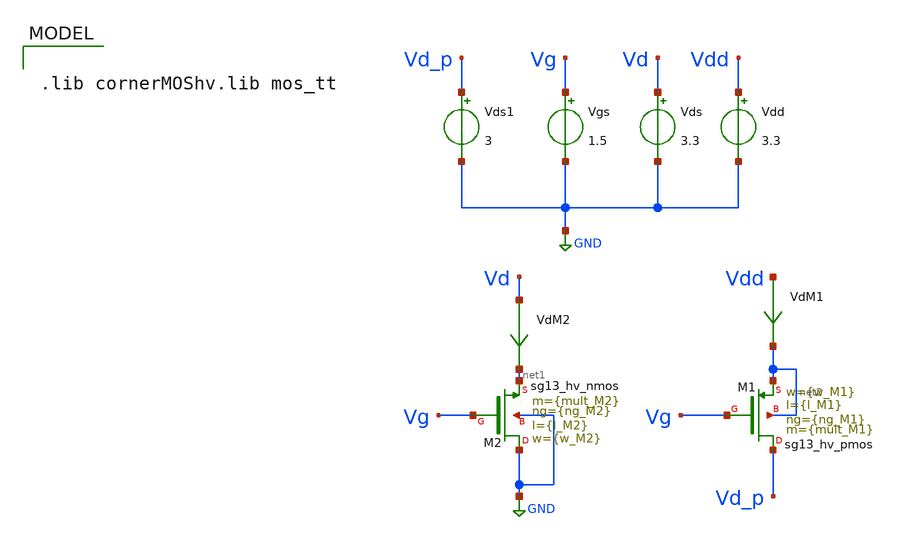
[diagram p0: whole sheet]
** sch_path: xschem/TB_hvMOS_POWER_Sizing.sch
**.subckt TB_hvMOS_POWER_Sizing
Vgs Vg GND 1.5
Vds Vd GND 3.3
Vdd Vdd GND 3.3
XM2 GND Vg net1 GND sg13_hv_nmos w={w_M2} l={l_M2} ng={ng_M2} m={mult_M2} mm_ok=1
VdM1 Vdd net2 0
.save i(vdm1)
XM1 Vd_p Vg net2 net2 sg13_hv_pmos w={w_M1} l={l_M1} ng={ng_M1} m={mult_M1} mm_ok=1
VdM2 Vd net1 0
.save i(vdm2)
Vds1 Vd_p GND 3
**** begin user architecture code

.lib cornerMOShv.lib mos_tt



.save all
* + @M.XM1.m1[id]  @n.xm1.nsg13_hv_pmos[vth]  @n.xm1.nsg13_hv_pmos[ad]  @n.xm2.nsg13_hv_nmos[vth]

.control
reset
alter Vgs 3.3
dc Vds 0 1 0.01
*dc Vds 0 0.5 0.01 temp 0 27 1
let Vds_M2 = v(Vd)
plot i(VdM2) vs Vds_M2

*meas DC Ron_M2 DERIV i(VdM2) AT=0.2
let I_M2 = i(VdM2)
let G_M2 = deriv(I_M2)
let Ron_M2 = 1/G_M2
plot Ron_M2
let VthM1_off =  @n.xm1.nsg13_hv_pmos[vth]
let VthM2 =  @n.xm2.nsg13_hv_nmos[vth]
*plot VthM1_off
*plot VthM2
.endc

.control
reset
alter Vgs 0
dc Vds1 2 3.3 0.01
*dc Vds 2 3.3 0.01 temp 0 27 1

plot i(VdM1)
let I_M1 = i(VdM1)
let G_M1 = deriv(I_M1)
let Ron_M1 = -1/G_M1
let Vsd_M1 = v(Vdd) -v(Vd_p)
plot Ron_M1 vs Vsd_M1
let VthM1_on = @n.xm1.nsg13_hv_pmos[vth]
*plot VthM1_on
.endc

.control
reset
alter Vgs 3.3
dc Vds1 0 3.3 0.01
plot i(VdM1)
let I_M1 = i(VdM1)
let G_M1 = deriv(I_M1)
let Ron_M1_subth = 1/G_M1
plot Ron_M1_subth

let VthM1_subth = @n.xm1.nsg13_hv_pmos[vth]
*plot VthM1_subth
.endc
.end




.param temp=27
.param mult_M1 = 2400
.param w_M1 =10u
*.param l_M1 = 0.2u ** Posee mayor capacidad de corriente, pero en sub-umbral conduce mucha
*+ corriente
.param l_M1 = 0.22u
.param ng_M1 = 1

.param mult_M2 = 1200
.param w_M2 =10u
*.param l_M2 =0.25u
.param l_M2 =0.25u
.param ng_M2 =1





**** end user architecture code
**.ends
.GLOBAL GND
.end
